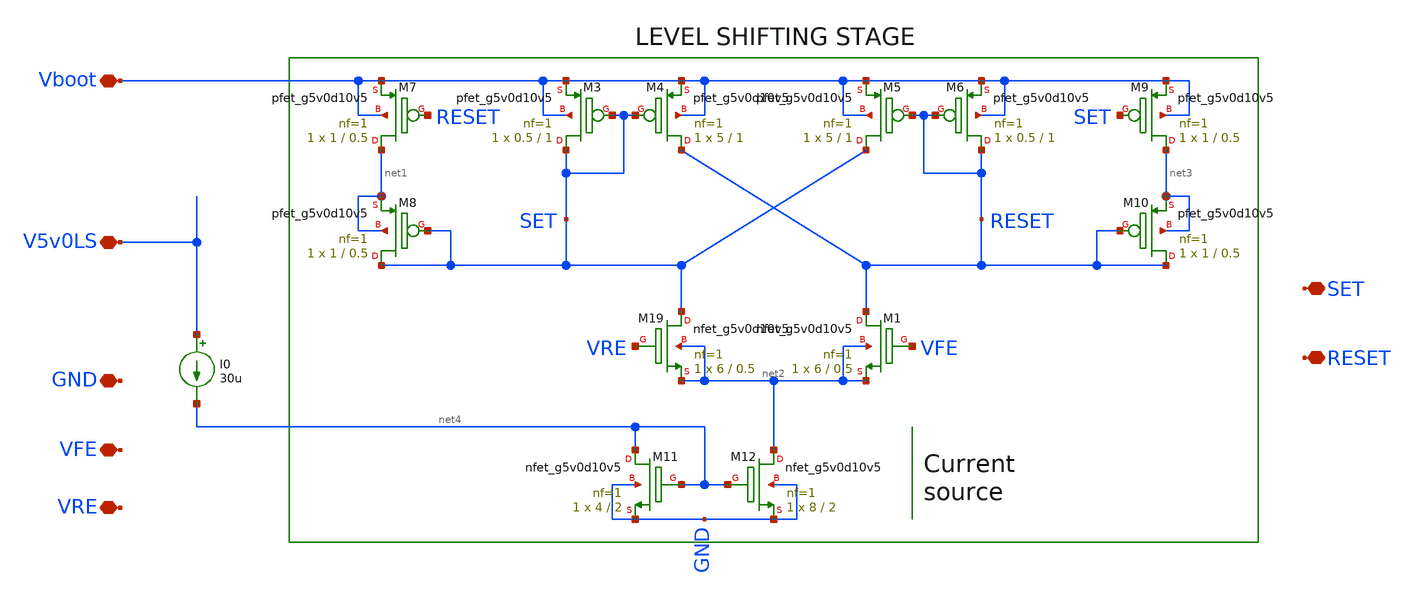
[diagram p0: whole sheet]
** sch_path: xschem/boot_ls_stage.sch
**.subckt boot_ls_stage V5v0LS GND Vboot VFE VRE SET RESET
*.iopin V5v0LS
*.iopin GND
*.iopin Vboot
*.iopin VFE
*.iopin VRE
*.iopin SET
*.iopin RESET
XM7 net1 RESET Vboot Vboot sky130_fd_pr__pfet_g5v0d10v5 L=0.5 W=1 nf=1 ad='int((nf+1)/2) * W/nf * 0.29'
+ as='int((nf+2)/2) * W/nf * 0.29' pd='2*int((nf+1)/2) * (W/nf + 0.29)' ps='2*int((nf+2)/2) * (W/nf + 0.29)'
+ nrd='0.29 / W' nrs='0.29 / W' sa=0 sb=0 sd=0 mult=1 m=1
XM8 SET SET net1 net1 sky130_fd_pr__pfet_g5v0d10v5 L=0.5 W=1 nf=1 ad='int((nf+1)/2) * W/nf * 0.29' as='int((nf+2)/2) * W/nf * 0.29'
+ pd='2*int((nf+1)/2) * (W/nf + 0.29)' ps='2*int((nf+2)/2) * (W/nf + 0.29)' nrd='0.29 / W' nrs='0.29 / W'
+ sa=0 sb=0 sd=0 mult=1 m=1
XM4 RESET SET Vboot Vboot sky130_fd_pr__pfet_g5v0d10v5 L=1 W=5 nf=1 ad='int((nf+1)/2) * W/nf * 0.29'
+ as='int((nf+2)/2) * W/nf * 0.29' pd='2*int((nf+1)/2) * (W/nf + 0.29)' ps='2*int((nf+2)/2) * (W/nf + 0.29)'
+ nrd='0.29 / W' nrs='0.29 / W' sa=0 sb=0 sd=0 mult=1 m=1
XM3 SET SET Vboot Vboot sky130_fd_pr__pfet_g5v0d10v5 L=1 W=0.5 nf=1 ad='int((nf+1)/2) * W/nf * 0.29'
+ as='int((nf+2)/2) * W/nf * 0.29' pd='2*int((nf+1)/2) * (W/nf + 0.29)' ps='2*int((nf+2)/2) * (W/nf + 0.29)'
+ nrd='0.29 / W' nrs='0.29 / W' sa=0 sb=0 sd=0 mult=1 m=1
XM9 net3 SET Vboot Vboot sky130_fd_pr__pfet_g5v0d10v5 L=0.5 W=1 nf=1 ad='int((nf+1)/2) * W/nf * 0.29'
+ as='int((nf+2)/2) * W/nf * 0.29' pd='2*int((nf+1)/2) * (W/nf + 0.29)' ps='2*int((nf+2)/2) * (W/nf + 0.29)'
+ nrd='0.29 / W' nrs='0.29 / W' sa=0 sb=0 sd=0 mult=1 m=1
XM10 RESET RESET net3 net3 sky130_fd_pr__pfet_g5v0d10v5 L=0.5 W=1 nf=1 ad='int((nf+1)/2) * W/nf * 0.29'
+ as='int((nf+2)/2) * W/nf * 0.29' pd='2*int((nf+1)/2) * (W/nf + 0.29)' ps='2*int((nf+2)/2) * (W/nf + 0.29)'
+ nrd='0.29 / W' nrs='0.29 / W' sa=0 sb=0 sd=0 mult=1 m=1
XM5 SET RESET Vboot Vboot sky130_fd_pr__pfet_g5v0d10v5 L=1 W=5 nf=1 ad='int((nf+1)/2) * W/nf * 0.29'
+ as='int((nf+2)/2) * W/nf * 0.29' pd='2*int((nf+1)/2) * (W/nf + 0.29)' ps='2*int((nf+2)/2) * (W/nf + 0.29)'
+ nrd='0.29 / W' nrs='0.29 / W' sa=0 sb=0 sd=0 mult=1 m=1
XM6 RESET RESET Vboot Vboot sky130_fd_pr__pfet_g5v0d10v5 L=1 W=0.5 nf=1 ad='int((nf+1)/2) * W/nf * 0.29'
+ as='int((nf+2)/2) * W/nf * 0.29' pd='2*int((nf+1)/2) * (W/nf + 0.29)' ps='2*int((nf+2)/2) * (W/nf + 0.29)'
+ nrd='0.29 / W' nrs='0.29 / W' sa=0 sb=0 sd=0 mult=1 m=1
I0 V5v0LS net4 30u
XM11 net4 net4 GND GND sky130_fd_pr__nfet_g5v0d10v5 L=2 W=4 nf=1 ad='int((nf+1)/2) * W/nf * 0.29' as='int((nf+2)/2) * W/nf * 0.29'
+ pd='2*int((nf+1)/2) * (W/nf + 0.29)' ps='2*int((nf+2)/2) * (W/nf + 0.29)' nrd='0.29 / W' nrs='0.29 / W'
+ sa=0 sb=0 sd=0 mult=1 m=1
XM12 net2 net4 GND GND sky130_fd_pr__nfet_g5v0d10v5 L=2 W=8 nf=1 ad='int((nf+1)/2) * W/nf * 0.29' as='int((nf+2)/2) * W/nf * 0.29'
+ pd='2*int((nf+1)/2) * (W/nf + 0.29)' ps='2*int((nf+2)/2) * (W/nf + 0.29)' nrd='0.29 / W' nrs='0.29 / W'
+ sa=0 sb=0 sd=0 mult=1 m=1
XM19 SET VRE net2 net2 sky130_fd_pr__nfet_g5v0d10v5 L=0.5 W=6 nf=1 ad='int((nf+1)/2) * W/nf * 0.29' as='int((nf+2)/2) * W/nf * 0.29'
+ pd='2*int((nf+1)/2) * (W/nf + 0.29)' ps='2*int((nf+2)/2) * (W/nf + 0.29)' nrd='0.29 / W' nrs='0.29 / W'
+ sa=0 sb=0 sd=0 mult=1 m=1
XM1 RESET VFE net2 net2 sky130_fd_pr__nfet_g5v0d10v5 L=0.5 W=6 nf=1 ad='int((nf+1)/2) * W/nf * 0.29'
+ as='int((nf+2)/2) * W/nf * 0.29' pd='2*int((nf+1)/2) * (W/nf + 0.29)' ps='2*int((nf+2)/2) * (W/nf + 0.29)'
+ nrd='0.29 / W' nrs='0.29 / W' sa=0 sb=0 sd=0 mult=1 m=1
**.ends
.end
